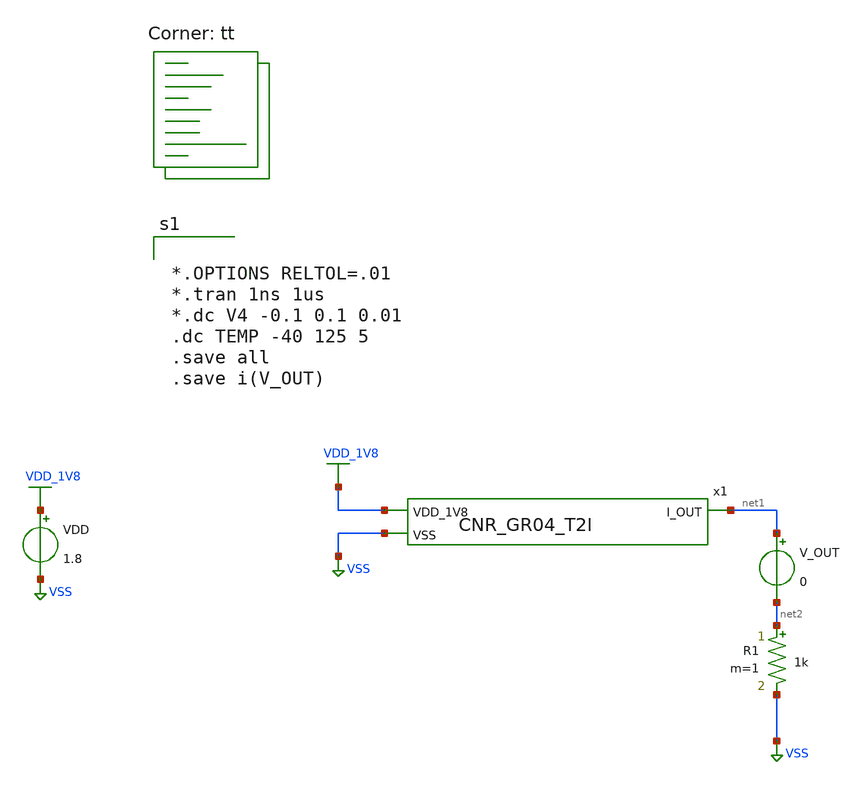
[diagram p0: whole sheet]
** sch_path: design/CNR_GR04_SKY130NM/CNR_GR04_T2I_SIM.sch
**.subckt CNR_GR04_T2I_SIM
x1 VDD_1V8 net1 VSS CNR_GR04_T2I
VDD VDD_1V8 VSS 1.8
V_OUT net1 net2 0
R1 net2 VSS 1k m=1
**** begin user architecture code


*.OPTIONS RELTOL=.01
*.tran 1ns 1us
*.dc V4 -0.1 0.1 0.01
.dc TEMP -40 125 5
.save all
.save i(V_OUT)


.lib $::SKYWATER_MODELS/sky130.lib.spice tt
**** end user architecture code
**.ends
.GLOBAL VDD_1V8
.GLOBAL VSS
.end
